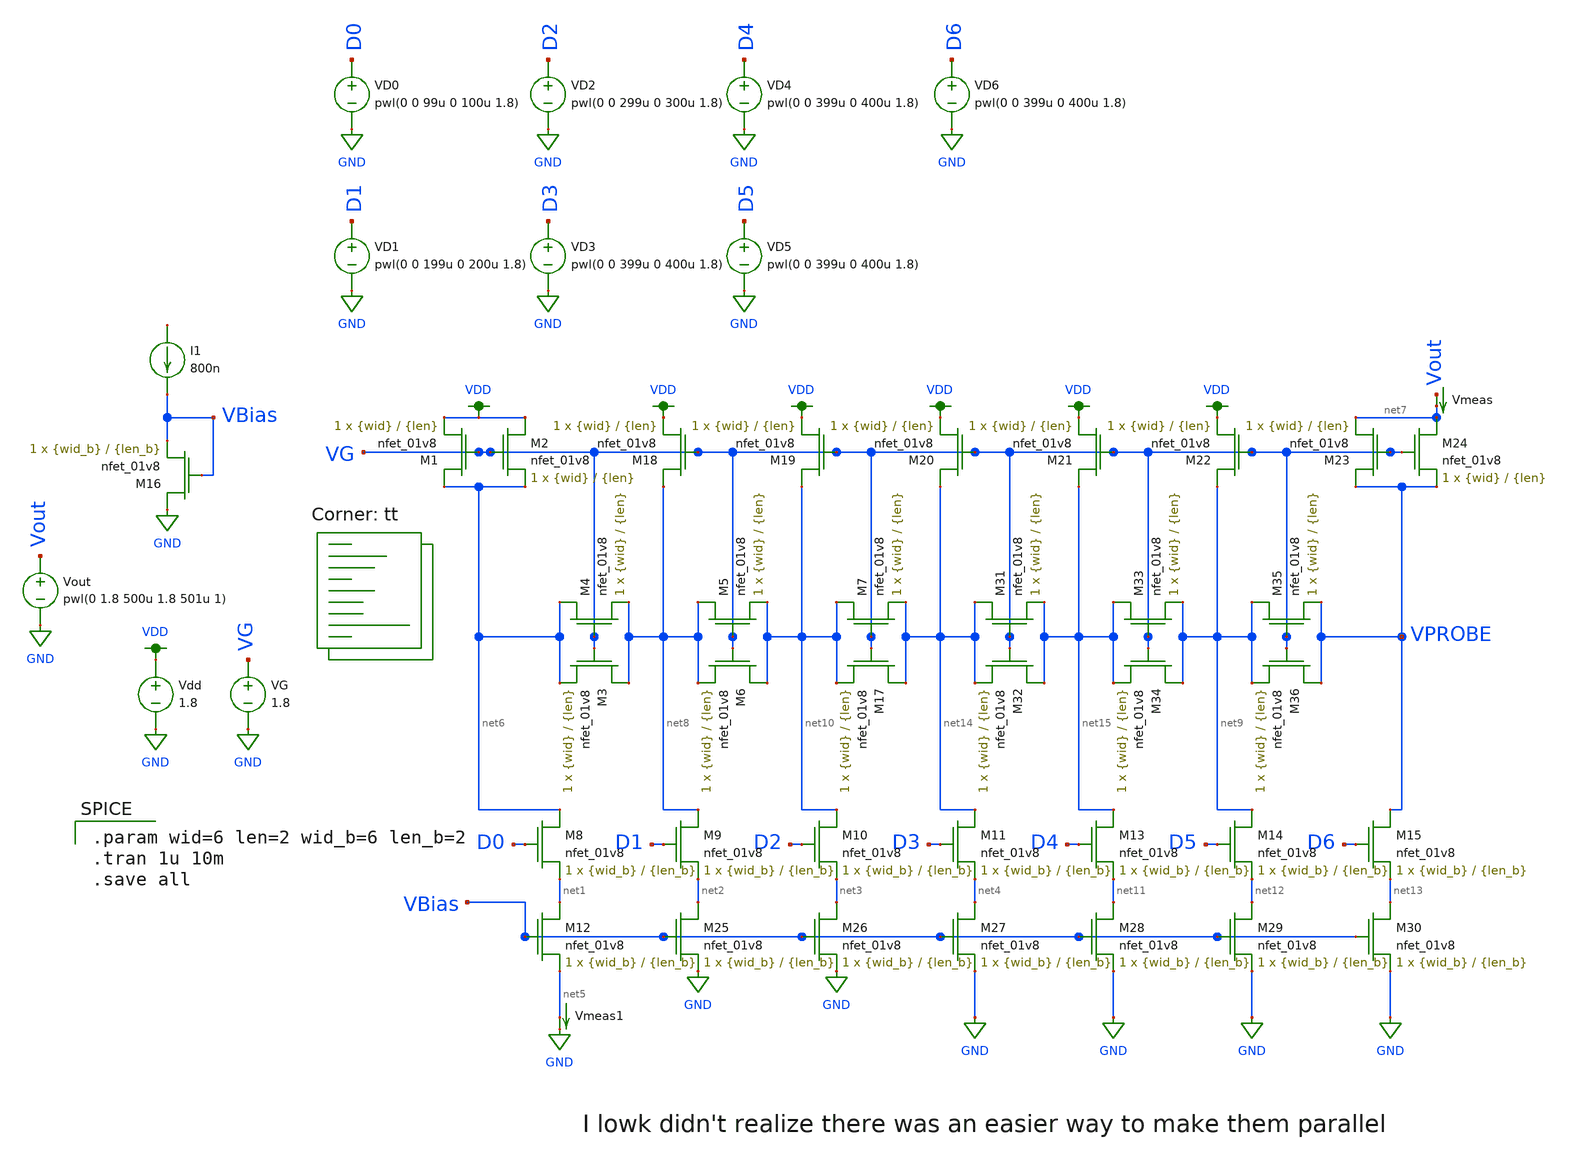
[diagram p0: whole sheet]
** sch_path: mp3/Reference Designs/ladder_tb.sch
**.subckt ladder_tb
XM8 net6 D0 net1 GND sky130_fd_pr__nfet_01v8 L={len_b} W={wid_b} nf=1 ad='int((nf+1)/2) * W/nf * 0.29'
+ as='int((nf+2)/2) * W/nf * 0.29' pd='2*int((nf+1)/2) * (W/nf + 0.29)' ps='2*int((nf+2)/2) * (W/nf + 0.29)'
+ nrd='0.29 / W' nrs='0.29 / W' sa=0 sb=0 sd=0 mult=1 m=1
Vmeas1 net5 GND 0
.save i(vmeas1)
Vdd VDD GND 1.8
VG VG GND 1.8
VD0 D0 GND pwl(0 0 99u 0 100u 1.8)
VD1 D1 GND pwl(0 0 199u 0 200u 1.8)
VD2 D2 GND pwl(0 0 299u 0 300u 1.8)
VD3 D3 GND pwl(0 0 399u 0 400u 1.8)
XM16 GND VBias VBias GND sky130_fd_pr__nfet_01v8 L={len_b} W={wid_b} nf=1 ad='int((nf+1)/2) * W/nf * 0.29'
+ as='int((nf+2)/2) * W/nf * 0.29' pd='2*int((nf+1)/2) * (W/nf + 0.29)' ps='2*int((nf+2)/2) * (W/nf + 0.29)'
+ nrd='0.29 / W' nrs='0.29 / W' sa=0 sb=0 sd=0 mult=1 m=1
I1 net16 VBias 800n
XM1 net6 VG VDD GND sky130_fd_pr__nfet_01v8 L={len} W={wid} nf=1 ad='int((nf+1)/2) * W/nf * 0.29' as='int((nf+2)/2) * W/nf * 0.29'
+ pd='2*int((nf+1)/2) * (W/nf + 0.29)' ps='2*int((nf+2)/2) * (W/nf + 0.29)' nrd='0.29 / W' nrs='0.29 / W'
+ sa=0 sb=0 sd=0 mult=1 m=1
XM4 net6 VG net8 GND sky130_fd_pr__nfet_01v8 L={len} W={wid} nf=1 ad='int((nf+1)/2) * W/nf * 0.29' as='int((nf+2)/2) * W/nf * 0.29'
+ pd='2*int((nf+1)/2) * (W/nf + 0.29)' ps='2*int((nf+2)/2) * (W/nf + 0.29)' nrd='0.29 / W' nrs='0.29 / W'
+ sa=0 sb=0 sd=0 mult=1 m=1
Vmeas Vout net7 0
.save i(vmeas)
VD4 D4 GND pwl(0 0 399u 0 400u 1.8)
VD5 D5 GND pwl(0 0 399u 0 400u 1.8)
VD6 D6 GND pwl(0 0 399u 0 400u 1.8)
XM12 net1 VBias net5 GND sky130_fd_pr__nfet_01v8 L={len_b} W={wid_b} nf=1 ad='int((nf+1)/2) * W/nf * 0.29'
+ as='int((nf+2)/2) * W/nf * 0.29' pd='2*int((nf+1)/2) * (W/nf + 0.29)' ps='2*int((nf+2)/2) * (W/nf + 0.29)'
+ nrd='0.29 / W' nrs='0.29 / W' sa=0 sb=0 sd=0 mult=1 m=1
XM9 net8 D1 net2 GND sky130_fd_pr__nfet_01v8 L={len_b} W={wid_b} nf=1 ad='int((nf+1)/2) * W/nf * 0.29'
+ as='int((nf+2)/2) * W/nf * 0.29' pd='2*int((nf+1)/2) * (W/nf + 0.29)' ps='2*int((nf+2)/2) * (W/nf + 0.29)'
+ nrd='0.29 / W' nrs='0.29 / W' sa=0 sb=0 sd=0 mult=1 m=1
XM10 net10 D2 net3 GND sky130_fd_pr__nfet_01v8 L={len_b} W={wid_b} nf=1 ad='int((nf+1)/2) * W/nf * 0.29'
+ as='int((nf+2)/2) * W/nf * 0.29' pd='2*int((nf+1)/2) * (W/nf + 0.29)' ps='2*int((nf+2)/2) * (W/nf + 0.29)'
+ nrd='0.29 / W' nrs='0.29 / W' sa=0 sb=0 sd=0 mult=1 m=1
XM11 net14 D3 net4 GND sky130_fd_pr__nfet_01v8 L={len_b} W={wid_b} nf=1 ad='int((nf+1)/2) * W/nf * 0.29'
+ as='int((nf+2)/2) * W/nf * 0.29' pd='2*int((nf+1)/2) * (W/nf + 0.29)' ps='2*int((nf+2)/2) * (W/nf + 0.29)'
+ nrd='0.29 / W' nrs='0.29 / W' sa=0 sb=0 sd=0 mult=1 m=1
XM13 net15 D4 net11 GND sky130_fd_pr__nfet_01v8 L={len_b} W={wid_b} nf=1 ad='int((nf+1)/2) * W/nf * 0.29'
+ as='int((nf+2)/2) * W/nf * 0.29' pd='2*int((nf+1)/2) * (W/nf + 0.29)' ps='2*int((nf+2)/2) * (W/nf + 0.29)'
+ nrd='0.29 / W' nrs='0.29 / W' sa=0 sb=0 sd=0 mult=1 m=1
XM14 net9 D5 net12 GND sky130_fd_pr__nfet_01v8 L={len_b} W={wid_b} nf=1 ad='int((nf+1)/2) * W/nf * 0.29'
+ as='int((nf+2)/2) * W/nf * 0.29' pd='2*int((nf+1)/2) * (W/nf + 0.29)' ps='2*int((nf+2)/2) * (W/nf + 0.29)'
+ nrd='0.29 / W' nrs='0.29 / W' sa=0 sb=0 sd=0 mult=1 m=1
XM15 VPROBE D6 net13 GND sky130_fd_pr__nfet_01v8 L={len_b} W={wid_b} nf=1 ad='int((nf+1)/2) * W/nf * 0.29'
+ as='int((nf+2)/2) * W/nf * 0.29' pd='2*int((nf+1)/2) * (W/nf + 0.29)' ps='2*int((nf+2)/2) * (W/nf + 0.29)'
+ nrd='0.29 / W' nrs='0.29 / W' sa=0 sb=0 sd=0 mult=1 m=1
XM25 net2 VBias GND GND sky130_fd_pr__nfet_01v8 L={len_b} W={wid_b} nf=1 ad='int((nf+1)/2) * W/nf * 0.29'
+ as='int((nf+2)/2) * W/nf * 0.29' pd='2*int((nf+1)/2) * (W/nf + 0.29)' ps='2*int((nf+2)/2) * (W/nf + 0.29)'
+ nrd='0.29 / W' nrs='0.29 / W' sa=0 sb=0 sd=0 mult=1 m=1
XM26 net3 VBias GND GND sky130_fd_pr__nfet_01v8 L={len_b} W={wid_b} nf=1 ad='int((nf+1)/2) * W/nf * 0.29'
+ as='int((nf+2)/2) * W/nf * 0.29' pd='2*int((nf+1)/2) * (W/nf + 0.29)' ps='2*int((nf+2)/2) * (W/nf + 0.29)'
+ nrd='0.29 / W' nrs='0.29 / W' sa=0 sb=0 sd=0 mult=1 m=1
XM27 net4 VBias GND GND sky130_fd_pr__nfet_01v8 L={len_b} W={wid_b} nf=1 ad='int((nf+1)/2) * W/nf * 0.29'
+ as='int((nf+2)/2) * W/nf * 0.29' pd='2*int((nf+1)/2) * (W/nf + 0.29)' ps='2*int((nf+2)/2) * (W/nf + 0.29)'
+ nrd='0.29 / W' nrs='0.29 / W' sa=0 sb=0 sd=0 mult=1 m=1
XM28 net11 VBias GND GND sky130_fd_pr__nfet_01v8 L={len_b} W={wid_b} nf=1 ad='int((nf+1)/2) * W/nf * 0.29'
+ as='int((nf+2)/2) * W/nf * 0.29' pd='2*int((nf+1)/2) * (W/nf + 0.29)' ps='2*int((nf+2)/2) * (W/nf + 0.29)'
+ nrd='0.29 / W' nrs='0.29 / W' sa=0 sb=0 sd=0 mult=1 m=1
XM29 net12 VBias GND GND sky130_fd_pr__nfet_01v8 L={len_b} W={wid_b} nf=1 ad='int((nf+1)/2) * W/nf * 0.29'
+ as='int((nf+2)/2) * W/nf * 0.29' pd='2*int((nf+1)/2) * (W/nf + 0.29)' ps='2*int((nf+2)/2) * (W/nf + 0.29)'
+ nrd='0.29 / W' nrs='0.29 / W' sa=0 sb=0 sd=0 mult=1 m=1
XM30 net13 VBias GND GND sky130_fd_pr__nfet_01v8 L={len_b} W={wid_b} nf=1 ad='int((nf+1)/2) * W/nf * 0.29'
+ as='int((nf+2)/2) * W/nf * 0.29' pd='2*int((nf+1)/2) * (W/nf + 0.29)' ps='2*int((nf+2)/2) * (W/nf + 0.29)'
+ nrd='0.29 / W' nrs='0.29 / W' sa=0 sb=0 sd=0 mult=1 m=1
XM2 VDD VG net6 GND sky130_fd_pr__nfet_01v8 L={len} W={wid} nf=1 ad='int((nf+1)/2) * W/nf * 0.29' as='int((nf+2)/2) * W/nf * 0.29'
+ pd='2*int((nf+1)/2) * (W/nf + 0.29)' ps='2*int((nf+2)/2) * (W/nf + 0.29)' nrd='0.29 / W' nrs='0.29 / W'
+ sa=0 sb=0 sd=0 mult=1 m=1
XM18 net8 VG VDD GND sky130_fd_pr__nfet_01v8 L={len} W={wid} nf=1 ad='int((nf+1)/2) * W/nf * 0.29' as='int((nf+2)/2) * W/nf * 0.29'
+ pd='2*int((nf+1)/2) * (W/nf + 0.29)' ps='2*int((nf+2)/2) * (W/nf + 0.29)' nrd='0.29 / W' nrs='0.29 / W'
+ sa=0 sb=0 sd=0 mult=1 m=1
XM19 net10 VG VDD GND sky130_fd_pr__nfet_01v8 L={len} W={wid} nf=1 ad='int((nf+1)/2) * W/nf * 0.29' as='int((nf+2)/2) * W/nf * 0.29'
+ pd='2*int((nf+1)/2) * (W/nf + 0.29)' ps='2*int((nf+2)/2) * (W/nf + 0.29)' nrd='0.29 / W' nrs='0.29 / W'
+ sa=0 sb=0 sd=0 mult=1 m=1
XM20 net14 VG VDD GND sky130_fd_pr__nfet_01v8 L={len} W={wid} nf=1 ad='int((nf+1)/2) * W/nf * 0.29' as='int((nf+2)/2) * W/nf * 0.29'
+ pd='2*int((nf+1)/2) * (W/nf + 0.29)' ps='2*int((nf+2)/2) * (W/nf + 0.29)' nrd='0.29 / W' nrs='0.29 / W'
+ sa=0 sb=0 sd=0 mult=1 m=1
XM21 net15 VG VDD GND sky130_fd_pr__nfet_01v8 L={len} W={wid} nf=1 ad='int((nf+1)/2) * W/nf * 0.29' as='int((nf+2)/2) * W/nf * 0.29'
+ pd='2*int((nf+1)/2) * (W/nf + 0.29)' ps='2*int((nf+2)/2) * (W/nf + 0.29)' nrd='0.29 / W' nrs='0.29 / W'
+ sa=0 sb=0 sd=0 mult=1 m=1
XM22 net9 VG VDD GND sky130_fd_pr__nfet_01v8 L={len} W={wid} nf=1 ad='int((nf+1)/2) * W/nf * 0.29' as='int((nf+2)/2) * W/nf * 0.29'
+ pd='2*int((nf+1)/2) * (W/nf + 0.29)' ps='2*int((nf+2)/2) * (W/nf + 0.29)' nrd='0.29 / W' nrs='0.29 / W'
+ sa=0 sb=0 sd=0 mult=1 m=1
XM23 VPROBE VG net7 GND sky130_fd_pr__nfet_01v8 L={len} W={wid} nf=1 ad='int((nf+1)/2) * W/nf * 0.29'
+ as='int((nf+2)/2) * W/nf * 0.29' pd='2*int((nf+1)/2) * (W/nf + 0.29)' ps='2*int((nf+2)/2) * (W/nf + 0.29)'
+ nrd='0.29 / W' nrs='0.29 / W' sa=0 sb=0 sd=0 mult=1 m=1
XM24 net7 VG VPROBE GND sky130_fd_pr__nfet_01v8 L={len} W={wid} nf=1 ad='int((nf+1)/2) * W/nf * 0.29'
+ as='int((nf+2)/2) * W/nf * 0.29' pd='2*int((nf+1)/2) * (W/nf + 0.29)' ps='2*int((nf+2)/2) * (W/nf + 0.29)'
+ nrd='0.29 / W' nrs='0.29 / W' sa=0 sb=0 sd=0 mult=1 m=1
XM3 net8 VG net6 GND sky130_fd_pr__nfet_01v8 L={len} W={wid} nf=1 ad='int((nf+1)/2) * W/nf * 0.29' as='int((nf+2)/2) * W/nf * 0.29'
+ pd='2*int((nf+1)/2) * (W/nf + 0.29)' ps='2*int((nf+2)/2) * (W/nf + 0.29)' nrd='0.29 / W' nrs='0.29 / W'
+ sa=0 sb=0 sd=0 mult=1 m=1
XM5 net8 VG net10 GND sky130_fd_pr__nfet_01v8 L={len} W={wid} nf=1 ad='int((nf+1)/2) * W/nf * 0.29' as='int((nf+2)/2) * W/nf * 0.29'
+ pd='2*int((nf+1)/2) * (W/nf + 0.29)' ps='2*int((nf+2)/2) * (W/nf + 0.29)' nrd='0.29 / W' nrs='0.29 / W'
+ sa=0 sb=0 sd=0 mult=1 m=1
XM6 net10 VG net8 GND sky130_fd_pr__nfet_01v8 L={len} W={wid} nf=1 ad='int((nf+1)/2) * W/nf * 0.29' as='int((nf+2)/2) * W/nf * 0.29'
+ pd='2*int((nf+1)/2) * (W/nf + 0.29)' ps='2*int((nf+2)/2) * (W/nf + 0.29)' nrd='0.29 / W' nrs='0.29 / W'
+ sa=0 sb=0 sd=0 mult=1 m=1
XM7 net10 VG net14 GND sky130_fd_pr__nfet_01v8 L={len} W={wid} nf=1 ad='int((nf+1)/2) * W/nf * 0.29'
+ as='int((nf+2)/2) * W/nf * 0.29' pd='2*int((nf+1)/2) * (W/nf + 0.29)' ps='2*int((nf+2)/2) * (W/nf + 0.29)'
+ nrd='0.29 / W' nrs='0.29 / W' sa=0 sb=0 sd=0 mult=1 m=1
XM17 net14 VG net10 GND sky130_fd_pr__nfet_01v8 L={len} W={wid} nf=1 ad='int((nf+1)/2) * W/nf * 0.29'
+ as='int((nf+2)/2) * W/nf * 0.29' pd='2*int((nf+1)/2) * (W/nf + 0.29)' ps='2*int((nf+2)/2) * (W/nf + 0.29)'
+ nrd='0.29 / W' nrs='0.29 / W' sa=0 sb=0 sd=0 mult=1 m=1
XM31 net14 VG net15 GND sky130_fd_pr__nfet_01v8 L={len} W={wid} nf=1 ad='int((nf+1)/2) * W/nf * 0.29'
+ as='int((nf+2)/2) * W/nf * 0.29' pd='2*int((nf+1)/2) * (W/nf + 0.29)' ps='2*int((nf+2)/2) * (W/nf + 0.29)'
+ nrd='0.29 / W' nrs='0.29 / W' sa=0 sb=0 sd=0 mult=1 m=1
XM32 net15 VG net14 GND sky130_fd_pr__nfet_01v8 L={len} W={wid} nf=1 ad='int((nf+1)/2) * W/nf * 0.29'
+ as='int((nf+2)/2) * W/nf * 0.29' pd='2*int((nf+1)/2) * (W/nf + 0.29)' ps='2*int((nf+2)/2) * (W/nf + 0.29)'
+ nrd='0.29 / W' nrs='0.29 / W' sa=0 sb=0 sd=0 mult=1 m=1
XM33 net15 VG net9 GND sky130_fd_pr__nfet_01v8 L={len} W={wid} nf=1 ad='int((nf+1)/2) * W/nf * 0.29'
+ as='int((nf+2)/2) * W/nf * 0.29' pd='2*int((nf+1)/2) * (W/nf + 0.29)' ps='2*int((nf+2)/2) * (W/nf + 0.29)'
+ nrd='0.29 / W' nrs='0.29 / W' sa=0 sb=0 sd=0 mult=1 m=1
XM34 net9 VG net15 GND sky130_fd_pr__nfet_01v8 L={len} W={wid} nf=1 ad='int((nf+1)/2) * W/nf * 0.29'
+ as='int((nf+2)/2) * W/nf * 0.29' pd='2*int((nf+1)/2) * (W/nf + 0.29)' ps='2*int((nf+2)/2) * (W/nf + 0.29)'
+ nrd='0.29 / W' nrs='0.29 / W' sa=0 sb=0 sd=0 mult=1 m=1
XM35 net9 VG VPROBE GND sky130_fd_pr__nfet_01v8 L={len} W={wid} nf=1 ad='int((nf+1)/2) * W/nf * 0.29'
+ as='int((nf+2)/2) * W/nf * 0.29' pd='2*int((nf+1)/2) * (W/nf + 0.29)' ps='2*int((nf+2)/2) * (W/nf + 0.29)'
+ nrd='0.29 / W' nrs='0.29 / W' sa=0 sb=0 sd=0 mult=1 m=1
XM36 VPROBE VG net9 GND sky130_fd_pr__nfet_01v8 L={len} W={wid} nf=1 ad='int((nf+1)/2) * W/nf * 0.29'
+ as='int((nf+2)/2) * W/nf * 0.29' pd='2*int((nf+1)/2) * (W/nf + 0.29)' ps='2*int((nf+2)/2) * (W/nf + 0.29)'
+ nrd='0.29 / W' nrs='0.29 / W' sa=0 sb=0 sd=0 mult=1 m=1
Vout Vout GND pwl(0 1.8 500u 1.8 501u 1)
**** begin user architecture code

.param wid=6 len=2 wid_b=6 len_b=2
.tran 1u 10m
.save all


.lib $::SKYWATER_MODELS/sky130.lib.spice tt
**** end user architecture code
**.ends
.GLOBAL GND
.GLOBAL VDD
.end
